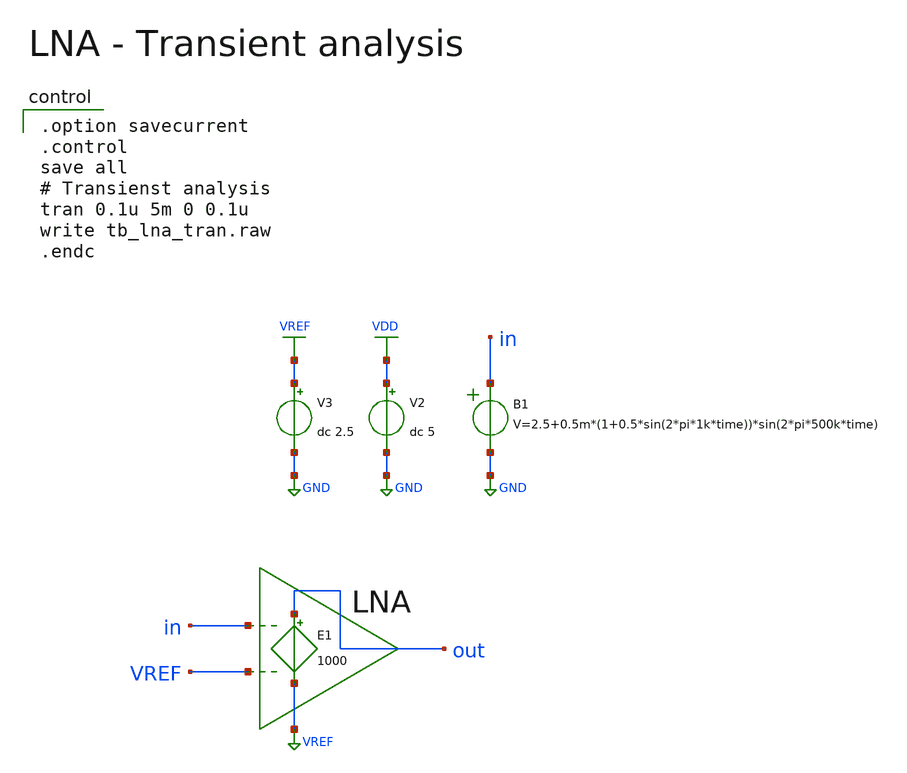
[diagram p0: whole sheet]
** sch_path: member_project/AM_Radio/Yamada3/xschem/tb_lna_tran.sch
**.subckt tb_lna_tran
V2 VDD GND dc 5
V3 VREF GND dc 2.5
B1 in GND V=2.5+0.5m*(1+0.5*sin(2*pi*1k*time))*sin(2*pi*500k*time)
E1 out VREF in VREF 1000
**** begin user architecture code

.option savecurrent
.control
save all
# Transienst analysis
tran 0.1u 5m 0 0.1u
write tb_lna_tran.raw
.endc

 .include $::LIB/ip62_models
**** end user architecture code
**.ends
.GLOBAL GND
.GLOBAL VDD
.GLOBAL VREF
.end
